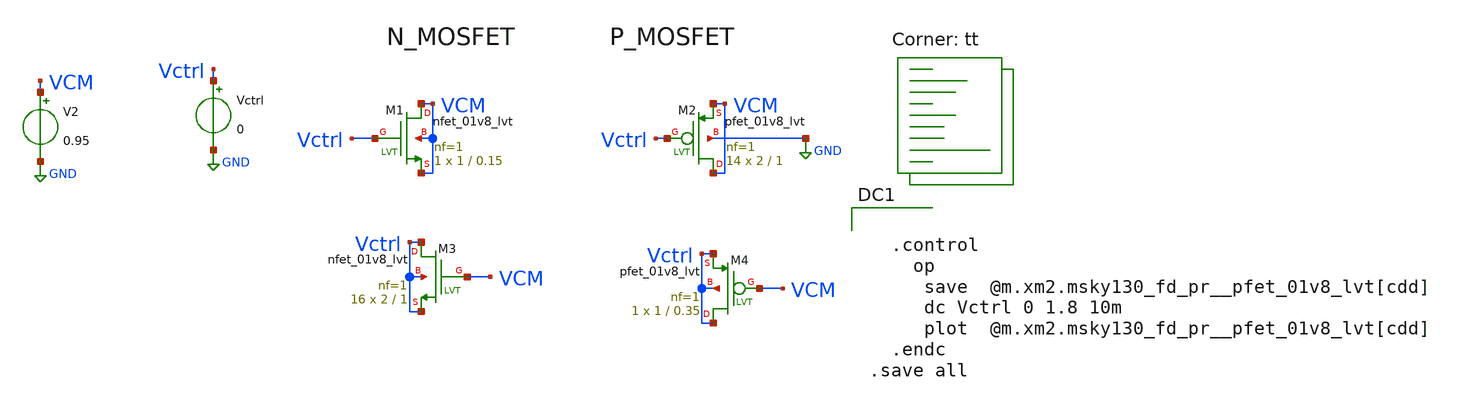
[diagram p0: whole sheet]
** sch_path: pll/lc_vco_lib_Hossam_Tarek/MOSCAPS_char/xschem/MOSCAPS_char.sch
**.subckt MOSCAPS_char
XM2 VCM Vctrl VCM GND sky130_fd_pr__pfet_01v8_lvt L=1 W=2 nf=1 ad='int((nf+1)/2) * W/nf * 0.29' as='int((nf+2)/2) * W/nf * 0.29'
+ pd='2*int((nf+1)/2) * (W/nf + 0.29)' ps='2*int((nf+2)/2) * (W/nf + 0.29)' nrd='0.29 / W' nrs='0.29 / W'
+ sa=0 sb=0 sd=0 mult=14 m=14
XM1 VCM Vctrl VCM VCM sky130_fd_pr__nfet_01v8_lvt L=0.15 W=1 nf=1 ad='int((nf+1)/2) * W/nf * 0.29' as='int((nf+2)/2) * W/nf * 0.29'
+ pd='2*int((nf+1)/2) * (W/nf + 0.29)' ps='2*int((nf+2)/2) * (W/nf + 0.29)' nrd='0.29 / W' nrs='0.29 / W'
+ sa=0 sb=0 sd=0 mult=1 m=1
Vctrl Vctrl GND 0
XM3 Vctrl VCM Vctrl Vctrl sky130_fd_pr__nfet_01v8_lvt L=1 W=2 nf=1 ad='int((nf+1)/2) * W/nf * 0.29' as='int((nf+2)/2) * W/nf * 0.29'
+ pd='2*int((nf+1)/2) * (W/nf + 0.29)' ps='2*int((nf+2)/2) * (W/nf + 0.29)' nrd='0.29 / W' nrs='0.29 / W'
+ sa=0 sb=0 sd=0 mult=16 m=16
XM4 Vctrl VCM Vctrl Vctrl sky130_fd_pr__pfet_01v8_lvt L=0.35 W=1 nf=1 ad='int((nf+1)/2) * W/nf * 0.29'
+ as='int((nf+2)/2) * W/nf * 0.29' pd='2*int((nf+1)/2) * (W/nf + 0.29)' ps='2*int((nf+2)/2) * (W/nf + 0.29)'
+ nrd='0.29 / W' nrs='0.29 / W' sa=0 sb=0 sd=0 mult=1 m=1
V2 VCM GND 0.95
**** begin user architecture code
.lib $::SKYWATER_MODELS/sky130.lib.spice tt


  .control
    op
     save  @m.xm2.msky130_fd_pr__pfet_01v8_lvt[cdd]
     dc Vctrl 0 1.8 10m
     plot  @m.xm2.msky130_fd_pr__pfet_01v8_lvt[cdd]
  .endc
.save all

**** end user architecture code
**.ends
.GLOBAL GND
.end
